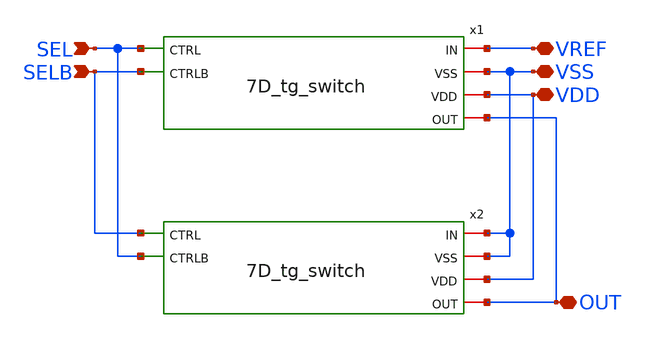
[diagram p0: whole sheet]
** sch_path: designs/libs/core_matchmaker/7D_ref_sel_2to1/7D_ref_sel_2to1.sch
**.subckt 7D_ref_sel_2to1 VREF VSS VDD OUT SEL SELB
*.iopin VREF
*.iopin VSS
*.iopin VDD
*.iopin OUT
*.ipin SEL
*.ipin SELB
x1 VREF VSS VDD SEL SELB OUT 7D_tg_switch
x2 VSS VSS VDD SELB SEL OUT 7D_tg_switch
**.ends
.end
